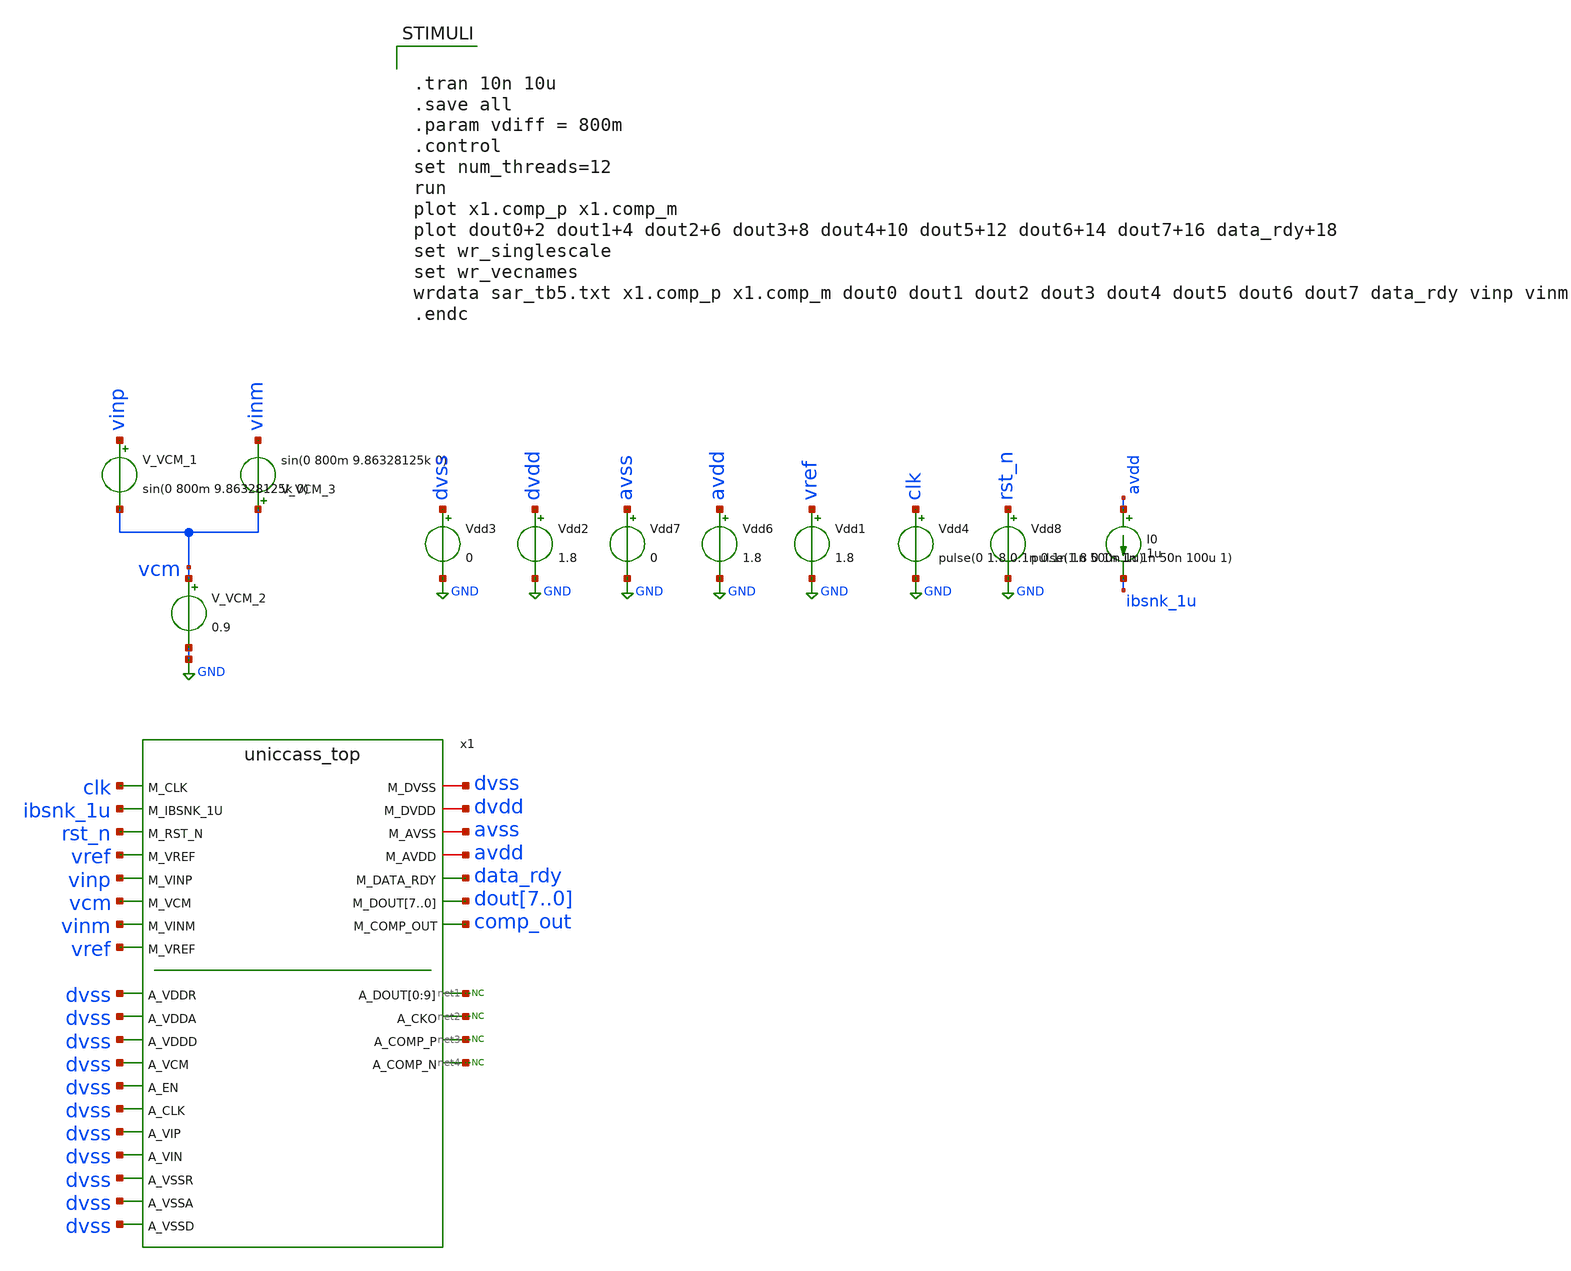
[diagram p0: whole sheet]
** sch_path: top/test/testbench/uniccass_top_tb.sch
.lib $::SKYWATER_MODELS/sky130.lib.spice tt
.include $::SKYWATER_STDCELLS/sky130_fd_sc_hd.spice

**.subckt uniccass_top_tb
Vdd8 rst_n GND pulse(1.8 0 1n 1n 1n 50n 100u 1)
Vdd4 clk GND pulse(0 1.8 0.1n 0.1n 1n 500n 1u)
Vdd1 vref GND 1.8
V_VCM_2 vcm GND 0.9
V_VCM_1 vinp vcm sin(0 800m 9.86328125k 0)
V_VCM_3 vcm vinm sin(0 800m 9.86328125k 0)
I0 avdd ibsnk_1u 1u
Vdd2 dvdd GND 1.8
Vdd3 dvss GND 0
Vdd6 avdd GND 1.8
Vdd7 avss GND 0
x1 dvss dvdd avss clk avdd ibsnk_1u rst_n vref vinp data_rdy vcm dout7 dout6 dout5 dout4 dout3 dout2
+ dout1 dout0 comp_out vinm dvss net1 net1 net1 net1 net1 net1 net1 net1 net1 net1 dvss net2 dvss net3 net4
+ dvss dvss dvss dvss dvss dvss dvss dvss uniccass_top
* noconn #net1
* noconn #net2
* noconn #net3
* noconn #net4
**** begin user architecture code


.tran 10n 10u
.save all
.param vdiff = 800m
.control
set num_threads=12
run
plot x1.comp_p x1.comp_m
plot dout0+2 dout1+4 dout2+6 dout3+8 dout4+10 dout5+12 dout6+14 dout7+16 data_rdy+18
set wr_singlescale
set wr_vecnames
wrdata sar_tb5.txt x1.comp_p x1.comp_m dout0 dout1 dout2 dout3 dout4 dout5 dout6 dout7 data_rdy vinp
+ vinm
.endc



.model SWITCH1 sw vt=0.9 vh=0 ron=1 roff =100G

**** end user architecture code
**.ends
.GLOBAL GND
.end
